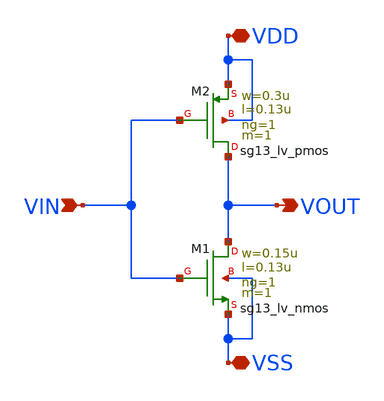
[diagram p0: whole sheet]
** sch_path: ADC8711-main/schematic/xschem/INV_D1.sch
**.subckt INV_D1 VDD VSS VOUT VIN
*.iopin VDD
*.iopin VSS
*.opin VOUT
*.ipin VIN
XM2 VOUT VIN VDD VDD sg13_lv_pmos w=0.3u l=0.13u ng=1 m=1 mm_ok=1
XM1 VOUT VIN VSS VSS sg13_lv_nmos w=0.15u l=0.13u ng=1 m=1 mm_ok=1
**.ends
.end
